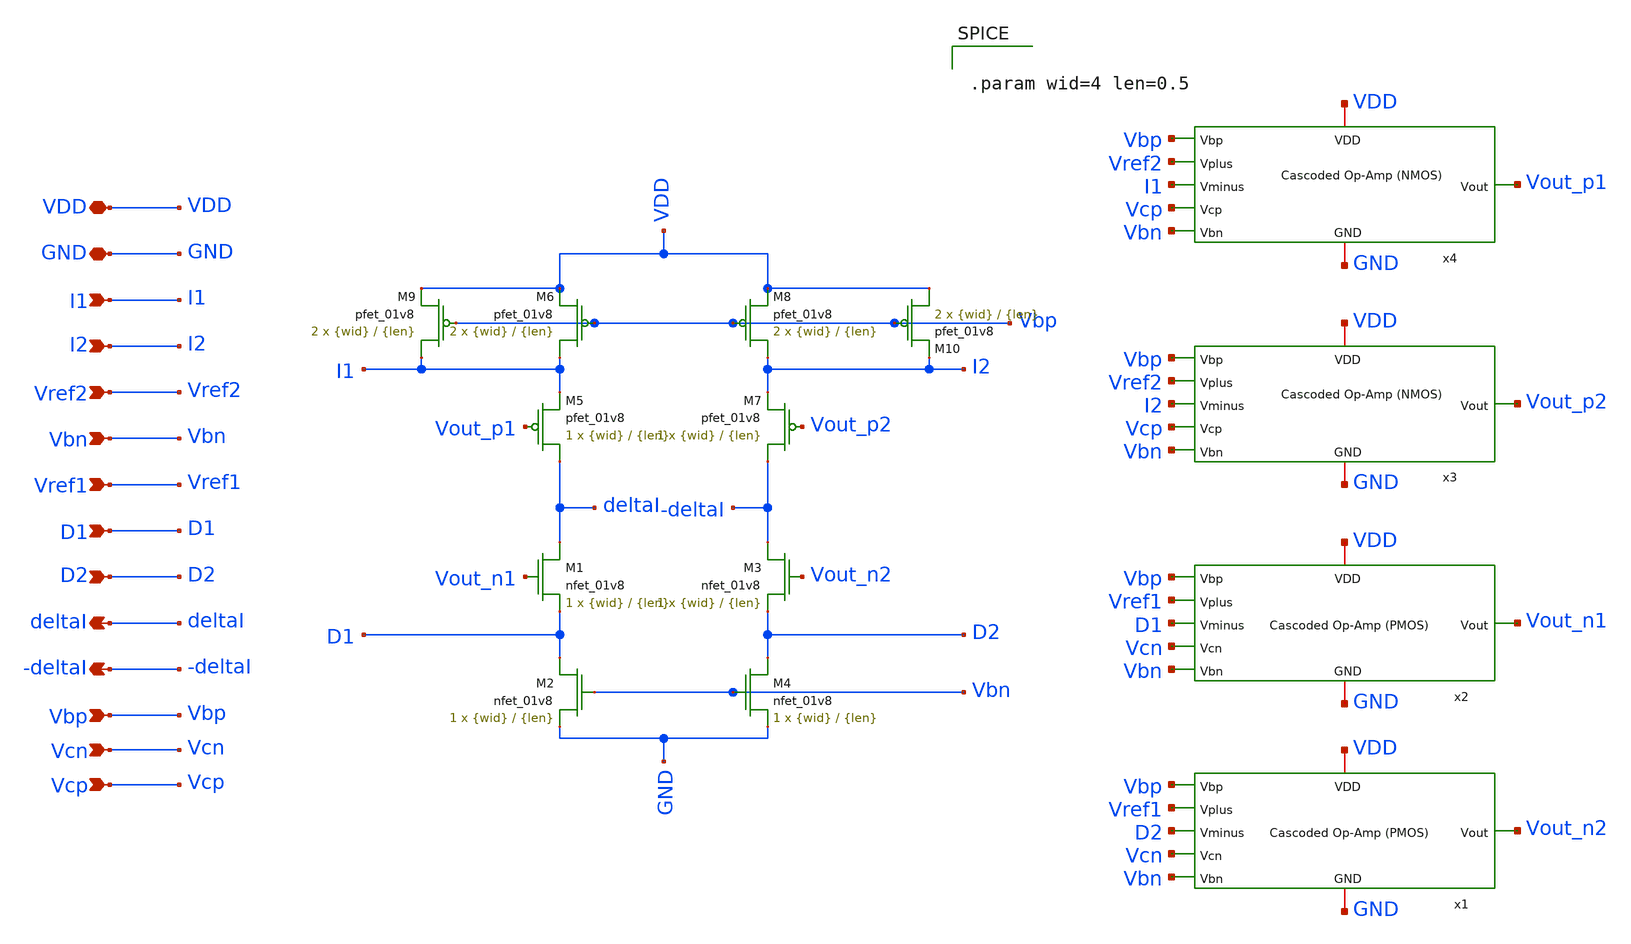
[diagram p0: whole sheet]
** sch_path: final/LDS/summation_LDS.sch
**.subckt summation_LDS VDD GND I1 I2 Vref2 Vbn Vref1 D1 D2 deltaI -deltaI Vbp Vcn Vcp
*.iopin VDD
*.iopin GND
*.ipin I1
*.ipin I2
*.ipin Vref2
*.ipin Vbn
*.ipin Vref1
*.ipin D1
*.ipin D2
*.opin deltaI
*.opin -deltaI
*.ipin Vbp
*.ipin Vcn
*.ipin Vcp
XM1 deltaI Vout_n1 D1 GND sky130_fd_pr__nfet_01v8 L={len} W={wid} nf=1 ad='int((nf+1)/2) * W/nf * 0.29'
+ as='int((nf+2)/2) * W/nf * 0.29' pd='2*int((nf+1)/2) * (W/nf + 0.29)' ps='2*int((nf+2)/2) * (W/nf + 0.29)'
+ nrd='0.29 / W' nrs='0.29 / W' sa=0 sb=0 sd=0 mult=1 m=1
XM3 -deltaI Vout_n2 D2 GND sky130_fd_pr__nfet_01v8 L={len} W={wid} nf=1 ad='int((nf+1)/2) * W/nf * 0.29'
+ as='int((nf+2)/2) * W/nf * 0.29' pd='2*int((nf+1)/2) * (W/nf + 0.29)' ps='2*int((nf+2)/2) * (W/nf + 0.29)'
+ nrd='0.29 / W' nrs='0.29 / W' sa=0 sb=0 sd=0 mult=1 m=1
XM5 deltaI Vout_p1 I1 VDD sky130_fd_pr__pfet_01v8 L={len} W={wid} nf=1 ad='int((nf+1)/2) * W/nf * 0.29'
+ as='int((nf+2)/2) * W/nf * 0.29' pd='2*int((nf+1)/2) * (W/nf + 0.29)' ps='2*int((nf+2)/2) * (W/nf + 0.29)'
+ nrd='0.29 / W' nrs='0.29 / W' sa=0 sb=0 sd=0 mult=1 m=1
XM7 -deltaI Vout_p2 I2 VDD sky130_fd_pr__pfet_01v8 L={len} W={wid} nf=1 ad='int((nf+1)/2) * W/nf * 0.29'
+ as='int((nf+2)/2) * W/nf * 0.29' pd='2*int((nf+1)/2) * (W/nf + 0.29)' ps='2*int((nf+2)/2) * (W/nf + 0.29)'
+ nrd='0.29 / W' nrs='0.29 / W' sa=0 sb=0 sd=0 mult=1 m=1
XM8 I2 Vbp VDD VDD sky130_fd_pr__pfet_01v8 L={len} W={wid} nf=1 ad='int((nf+1)/2) * W/nf * 0.29' as='int((nf+2)/2) * W/nf * 0.29'
+ pd='2*int((nf+1)/2) * (W/nf + 0.29)' ps='2*int((nf+2)/2) * (W/nf + 0.29)' nrd='0.29 / W' nrs='0.29 / W'
+ sa=0 sb=0 sd=0 mult=2 m=2
XM2 D1 Vbn GND GND sky130_fd_pr__nfet_01v8 L={len} W={wid} nf=1 ad='int((nf+1)/2) * W/nf * 0.29' as='int((nf+2)/2) * W/nf * 0.29'
+ pd='2*int((nf+1)/2) * (W/nf + 0.29)' ps='2*int((nf+2)/2) * (W/nf + 0.29)' nrd='0.29 / W' nrs='0.29 / W'
+ sa=0 sb=0 sd=0 mult=1 m=1
XM4 D2 Vbn GND GND sky130_fd_pr__nfet_01v8 L={len} W={wid} nf=1 ad='int((nf+1)/2) * W/nf * 0.29' as='int((nf+2)/2) * W/nf * 0.29'
+ pd='2*int((nf+1)/2) * (W/nf + 0.29)' ps='2*int((nf+2)/2) * (W/nf + 0.29)' nrd='0.29 / W' nrs='0.29 / W'
+ sa=0 sb=0 sd=0 mult=1 m=1
XM6 I1 Vbp VDD VDD sky130_fd_pr__pfet_01v8 L={len} W={wid} nf=1 ad='int((nf+1)/2) * W/nf * 0.29' as='int((nf+2)/2) * W/nf * 0.29'
+ pd='2*int((nf+1)/2) * (W/nf + 0.29)' ps='2*int((nf+2)/2) * (W/nf + 0.29)' nrd='0.29 / W' nrs='0.29 / W'
+ sa=0 sb=0 sd=0 mult=2 m=2
XM9 I1 Vbp VDD VDD sky130_fd_pr__pfet_01v8 L={len} W={wid} nf=1 ad='int((nf+1)/2) * W/nf * 0.29' as='int((nf+2)/2) * W/nf * 0.29'
+ pd='2*int((nf+1)/2) * (W/nf + 0.29)' ps='2*int((nf+2)/2) * (W/nf + 0.29)' nrd='0.29 / W' nrs='0.29 / W'
+ sa=0 sb=0 sd=0 mult=2 m=2
XM10 VDD Vbp I2 VDD sky130_fd_pr__pfet_01v8 L={len} W={wid} nf=1 ad='int((nf+1)/2) * W/nf * 0.29' as='int((nf+2)/2) * W/nf * 0.29'
+ pd='2*int((nf+1)/2) * (W/nf + 0.29)' ps='2*int((nf+2)/2) * (W/nf + 0.29)' nrd='0.29 / W' nrs='0.29 / W'
+ sa=0 sb=0 sd=0 mult=2 m=2
x1 Vbp Vref1 D2 Vcn Vbn VDD GND Vout_n2 cascoded_opamp_pmos_LDS
x2 Vbp Vref1 D1 Vcn Vbn VDD GND Vout_n1 cascoded_opamp_pmos_LDS
x3 Vbp Vref2 I2 Vcp Vbn VDD GND Vout_p2 cascoded_opamp_LDS
x4 Vbp Vref2 I1 Vcp Vbn VDD GND Vout_p1 cascoded_opamp_LDS
**** begin user architecture code


.param wid=4 len=0.5


**** end user architecture code
**.ends
.end
